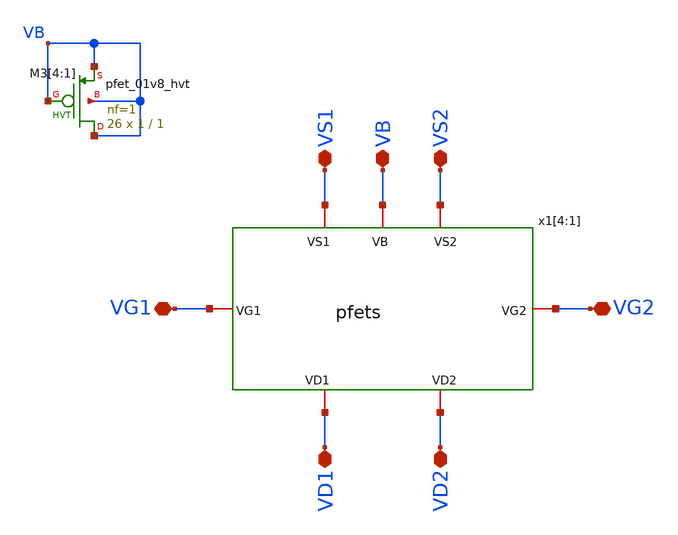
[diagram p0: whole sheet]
** sch_path: xschem/INA_layout_v2/pfets_4x.sch
**.subckt pfets_4x VS1 VS2 VB VG1 VG2 VD1 VD2
*.iopin VS1
*.iopin VS2
*.iopin VB
*.iopin VG1
*.iopin VG2
*.iopin VD1
*.iopin VD2
XM3[4] VB VB VB VB sky130_fd_pr__pfet_01v8_hvt L=1 W=1 nf=1 ad='int((nf+1)/2) * W/nf * 0.29' as='int((nf+2)/2) * W/nf * 0.29'
+ pd='2*int((nf+1)/2) * (W/nf + 0.29)' ps='2*int((nf+2)/2) * (W/nf + 0.29)' nrd='0.29 / W' nrs='0.29 / W'
+ sa=0 sb=0 sd=0 mult=26 m=26
XM3[3] VB VB VB VB sky130_fd_pr__pfet_01v8_hvt L=1 W=1 nf=1 ad='int((nf+1)/2) * W/nf * 0.29' as='int((nf+2)/2) * W/nf * 0.29'
+ pd='2*int((nf+1)/2) * (W/nf + 0.29)' ps='2*int((nf+2)/2) * (W/nf + 0.29)' nrd='0.29 / W' nrs='0.29 / W'
+ sa=0 sb=0 sd=0 mult=26 m=26
XM3[2] VB VB VB VB sky130_fd_pr__pfet_01v8_hvt L=1 W=1 nf=1 ad='int((nf+1)/2) * W/nf * 0.29' as='int((nf+2)/2) * W/nf * 0.29'
+ pd='2*int((nf+1)/2) * (W/nf + 0.29)' ps='2*int((nf+2)/2) * (W/nf + 0.29)' nrd='0.29 / W' nrs='0.29 / W'
+ sa=0 sb=0 sd=0 mult=26 m=26
XM3[1] VB VB VB VB sky130_fd_pr__pfet_01v8_hvt L=1 W=1 nf=1 ad='int((nf+1)/2) * W/nf * 0.29' as='int((nf+2)/2) * W/nf * 0.29'
+ pd='2*int((nf+1)/2) * (W/nf + 0.29)' ps='2*int((nf+2)/2) * (W/nf + 0.29)' nrd='0.29 / W' nrs='0.29 / W'
+ sa=0 sb=0 sd=0 mult=26 m=26
x1[4] VS1 VS2 VG2 VB VG1 VD2 VD1 pfets
x1[3] VS1 VS2 VG2 VB VG1 VD2 VD1 pfets
x1[2] VS1 VS2 VG2 VB VG1 VD2 VD1 pfets
x1[1] VS1 VS2 VG2 VB VG1 VD2 VD1 pfets
**.ends

* expanding   symbol:  INA_layout_v2/pfets.sym # of pins=7
** sym_path: INA_layout_v2/pfets.sym
** sch_path: INA_layout_v2/pfets.sch
.subckt pfets VS1 VS2 VG2 VB VG1 VD2 VD1
*.iopin VS1
*.iopin VS2
*.iopin VB
*.iopin VG1
*.iopin VG2
*.iopin VD1
*.iopin VD2
XM1 VD1 VG1 VS1 VB sky130_fd_pr__pfet_01v8_hvt L=1 W=1 nf=1 ad='int((nf+1)/2) * W/nf * 0.29' as='int((nf+2)/2) * W/nf * 0.29'
+ pd='2*int((nf+1)/2) * (W/nf + 0.29)' ps='2*int((nf+2)/2) * (W/nf + 0.29)' nrd='0.29 / W' nrs='0.29 / W'
+ sa=0 sb=0 sd=0 mult=22 m=22
XM2 VD2 VG2 VS2 VB sky130_fd_pr__pfet_01v8_hvt L=1 W=1 nf=1 ad='int((nf+1)/2) * W/nf * 0.29' as='int((nf+2)/2) * W/nf * 0.29'
+ pd='2*int((nf+1)/2) * (W/nf + 0.29)' ps='2*int((nf+2)/2) * (W/nf + 0.29)' nrd='0.29 / W' nrs='0.29 / W'
+ sa=0 sb=0 sd=0 mult=22 m=22
XM3[1] VB VB VB VB sky130_fd_pr__pfet_01v8_hvt L=1 W=1 nf=1 ad='int((nf+1)/2) * W/nf * 0.29' as='int((nf+2)/2) * W/nf * 0.29'
+ pd='2*int((nf+1)/2) * (W/nf + 0.29)' ps='2*int((nf+2)/2) * (W/nf + 0.29)' nrd='0.29 / W' nrs='0.29 / W'
+ sa=0 sb=0 sd=0 mult=4 m=4
XM3[0] VB VB VB VB sky130_fd_pr__pfet_01v8_hvt L=1 W=1 nf=1 ad='int((nf+1)/2) * W/nf * 0.29' as='int((nf+2)/2) * W/nf * 0.29'
+ pd='2*int((nf+1)/2) * (W/nf + 0.29)' ps='2*int((nf+2)/2) * (W/nf + 0.29)' nrd='0.29 / W' nrs='0.29 / W'
+ sa=0 sb=0 sd=0 mult=4 m=4
.ends

.end
